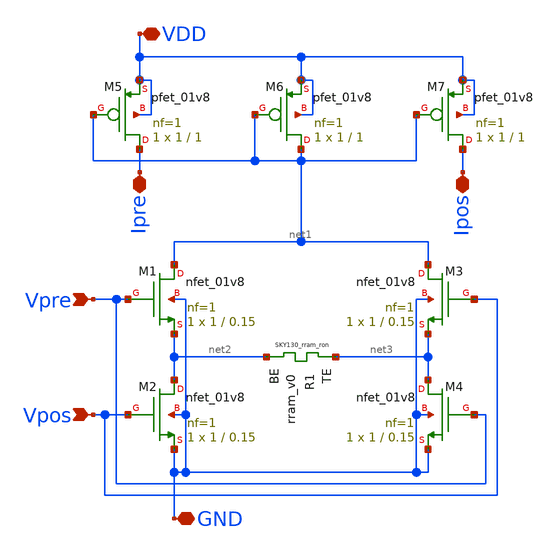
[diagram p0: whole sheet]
** sch_path: synapse/7T1R.sch
**.subckt 7T1R Vpre Vpos GND Ipre Ipos VDD
*.ipin Vpre
*.ipin Vpos
*.iopin GND
*.iopin Ipre
*.iopin Ipos
*.iopin VDD
XM1 net1 Vpre net2 GND sky130_fd_pr__nfet_01v8 L=0.15 W=1 nf=1 ad='int((nf+1)/2) * W/nf * 0.29' as='int((nf+2)/2) * W/nf * 0.29'
+ pd='2*int((nf+1)/2) * (W/nf + 0.29)' ps='2*int((nf+2)/2) * (W/nf + 0.29)' nrd='0.29 / W' nrs='0.29 / W'
+ sa=0 sb=0 sd=0 mult=1 m=1
XR1 net3 net2 rram_v0
XM2 net2 Vpos GND GND sky130_fd_pr__nfet_01v8 L=0.15 W=1 nf=1 ad='int((nf+1)/2) * W/nf * 0.29' as='int((nf+2)/2) * W/nf * 0.29'
+ pd='2*int((nf+1)/2) * (W/nf + 0.29)' ps='2*int((nf+2)/2) * (W/nf + 0.29)' nrd='0.29 / W' nrs='0.29 / W'
+ sa=0 sb=0 sd=0 mult=1 m=1
XM3 net1 Vpos net3 GND sky130_fd_pr__nfet_01v8 L=0.15 W=1 nf=1 ad='int((nf+1)/2) * W/nf * 0.29' as='int((nf+2)/2) * W/nf * 0.29'
+ pd='2*int((nf+1)/2) * (W/nf + 0.29)' ps='2*int((nf+2)/2) * (W/nf + 0.29)' nrd='0.29 / W' nrs='0.29 / W'
+ sa=0 sb=0 sd=0 mult=1 m=1
XM4 net3 Vpre GND GND sky130_fd_pr__nfet_01v8 L=0.15 W=1 nf=1 ad='int((nf+1)/2) * W/nf * 0.29' as='int((nf+2)/2) * W/nf * 0.29'
+ pd='2*int((nf+1)/2) * (W/nf + 0.29)' ps='2*int((nf+2)/2) * (W/nf + 0.29)' nrd='0.29 / W' nrs='0.29 / W'
+ sa=0 sb=0 sd=0 mult=1 m=1
XM5 Ipre net1 VDD VDD sky130_fd_pr__pfet_01v8 L=1 W=1 nf=1 ad='int((nf+1)/2) * W/nf * 0.29' as='int((nf+2)/2) * W/nf * 0.29'
+ pd='2*int((nf+1)/2) * (W/nf + 0.29)' ps='2*int((nf+2)/2) * (W/nf + 0.29)' nrd='0.29 / W' nrs='0.29 / W'
+ sa=0 sb=0 sd=0 mult=1 m=1
XM6 net1 net1 VDD VDD sky130_fd_pr__pfet_01v8 L=1 W=1 nf=1 ad='int((nf+1)/2) * W/nf * 0.29' as='int((nf+2)/2) * W/nf * 0.29'
+ pd='2*int((nf+1)/2) * (W/nf + 0.29)' ps='2*int((nf+2)/2) * (W/nf + 0.29)' nrd='0.29 / W' nrs='0.29 / W'
+ sa=0 sb=0 sd=0 mult=1 m=1
XM7 Ipos net1 VDD VDD sky130_fd_pr__pfet_01v8 L=1 W=1 nf=1 ad='int((nf+1)/2) * W/nf * 0.29' as='int((nf+2)/2) * W/nf * 0.29'
+ pd='2*int((nf+1)/2) * (W/nf + 0.29)' ps='2*int((nf+2)/2) * (W/nf + 0.29)' nrd='0.29 / W' nrs='0.29 / W'
+ sa=0 sb=0 sd=0 mult=1 m=1
**.ends
.end
